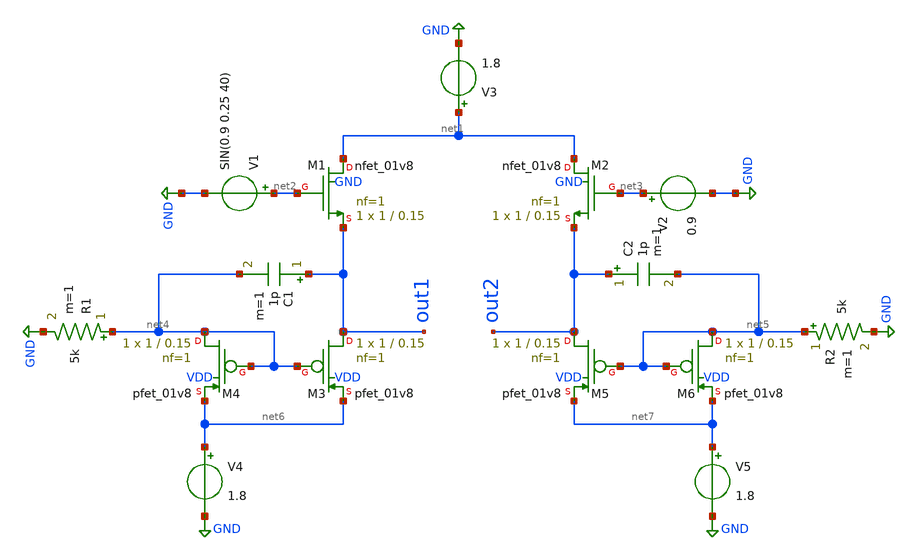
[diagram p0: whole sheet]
** sch_path: xschem/powerdetector/rms-detector.sch
**.subckt rms-detector
XM1 net1 net2 out1 GND sky130_fd_pr__nfet_01v8 L=0.15 W=1 nf=1 ad='int((nf+1)/2) * W/nf * 0.29' as='int((nf+2)/2) * W/nf * 0.29'
+ pd='2*int((nf+1)/2) * (W/nf + 0.29)' ps='2*int((nf+2)/2) * (W/nf + 0.29)' nrd='0.29 / W' nrs='0.29 / W'
+ sa=0 sb=0 sd=0 mult=1 m=1
XM2 net1 net3 out2 GND sky130_fd_pr__nfet_01v8 L=0.15 W=1 nf=1 ad='int((nf+1)/2) * W/nf * 0.29' as='int((nf+2)/2) * W/nf * 0.29'
+ pd='2*int((nf+1)/2) * (W/nf + 0.29)' ps='2*int((nf+2)/2) * (W/nf + 0.29)' nrd='0.29 / W' nrs='0.29 / W'
+ sa=0 sb=0 sd=0 mult=1 m=1
V1 net2 GND SIN(0.9 0.25 40)
V2 net3 GND 0.9
V3 net1 GND 1.8
XM3 out1 net4 net6 VDD sky130_fd_pr__pfet_01v8 L=0.15 W=1 nf=1 ad='int((nf+1)/2) * W/nf * 0.29' as='int((nf+2)/2) * W/nf * 0.29'
+ pd='2*int((nf+1)/2) * (W/nf + 0.29)' ps='2*int((nf+2)/2) * (W/nf + 0.29)' nrd='0.29 / W' nrs='0.29 / W'
+ sa=0 sb=0 sd=0 mult=1 m=1
XM4 net4 net4 net6 VDD sky130_fd_pr__pfet_01v8 L=0.15 W=1 nf=1 ad='int((nf+1)/2) * W/nf * 0.29' as='int((nf+2)/2) * W/nf * 0.29'
+ pd='2*int((nf+1)/2) * (W/nf + 0.29)' ps='2*int((nf+2)/2) * (W/nf + 0.29)' nrd='0.29 / W' nrs='0.29 / W'
+ sa=0 sb=0 sd=0 mult=1 m=1
XM5 out2 net5 net7 VDD sky130_fd_pr__pfet_01v8 L=0.15 W=1 nf=1 ad='int((nf+1)/2) * W/nf * 0.29' as='int((nf+2)/2) * W/nf * 0.29'
+ pd='2*int((nf+1)/2) * (W/nf + 0.29)' ps='2*int((nf+2)/2) * (W/nf + 0.29)' nrd='0.29 / W' nrs='0.29 / W'
+ sa=0 sb=0 sd=0 mult=1 m=1
XM6 net5 net5 net7 VDD sky130_fd_pr__pfet_01v8 L=0.15 W=1 nf=1 ad='int((nf+1)/2) * W/nf * 0.29' as='int((nf+2)/2) * W/nf * 0.29'
+ pd='2*int((nf+1)/2) * (W/nf + 0.29)' ps='2*int((nf+2)/2) * (W/nf + 0.29)' nrd='0.29 / W' nrs='0.29 / W'
+ sa=0 sb=0 sd=0 mult=1 m=1
V4 net6 GND 1.8
V5 net7 GND 1.8
R1 net4 GND 5k m=1
R2 net5 GND 5k m=1
C1 out1 net4 1p m=1
C2 out2 net5 1p m=1
**** begin user architecture code
 ** manual skywater pdks install (with patches applied)
* .lib $::SKYWATER_MODELS/models/sky130.lib.spice tt

** opencircuitdesign pdks install
.lib $::SKYWATER_MODELS/sky130.lib.spice tt

.param mc_mm_switch=0
.param mc_pr_switch=0



.tran 0.001s 0.1
.control
  run
.endc
.save all


**** end user architecture code
**.ends
.GLOBAL GND
.end
